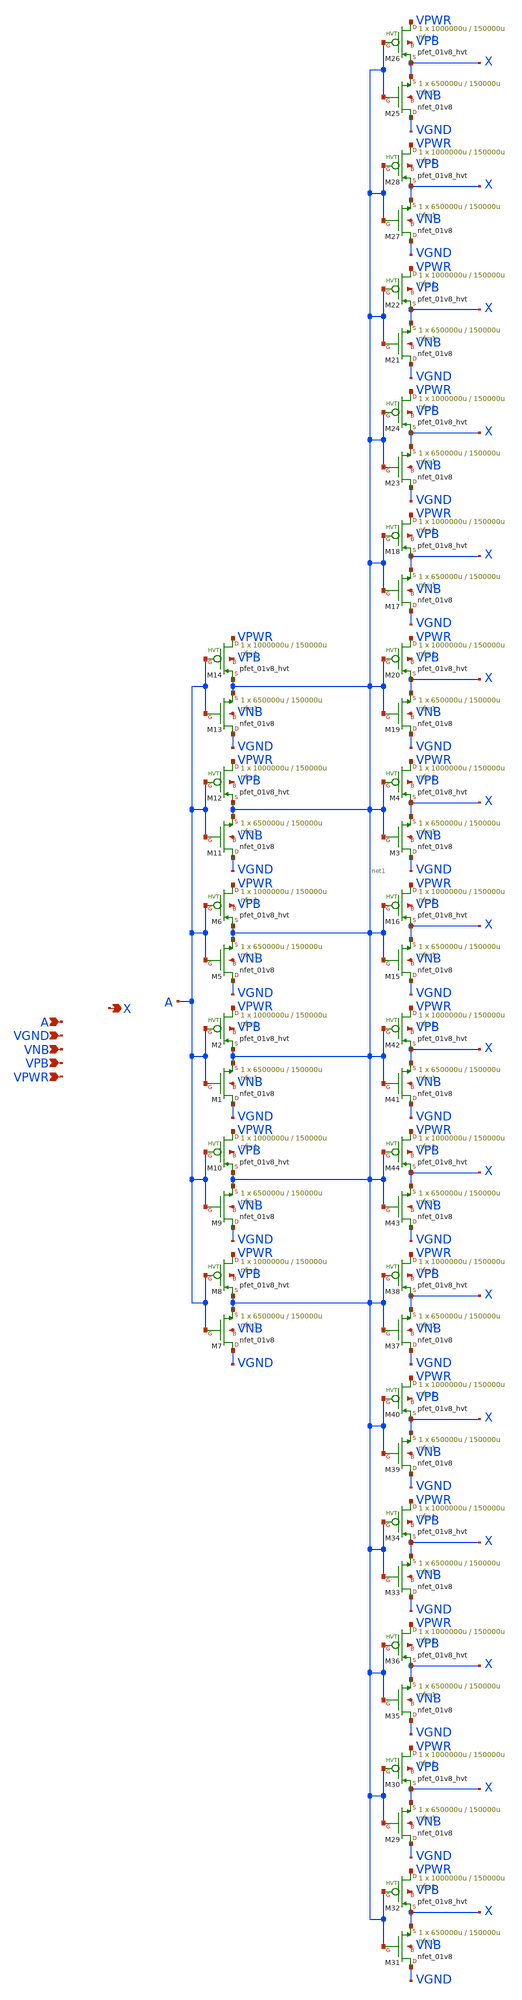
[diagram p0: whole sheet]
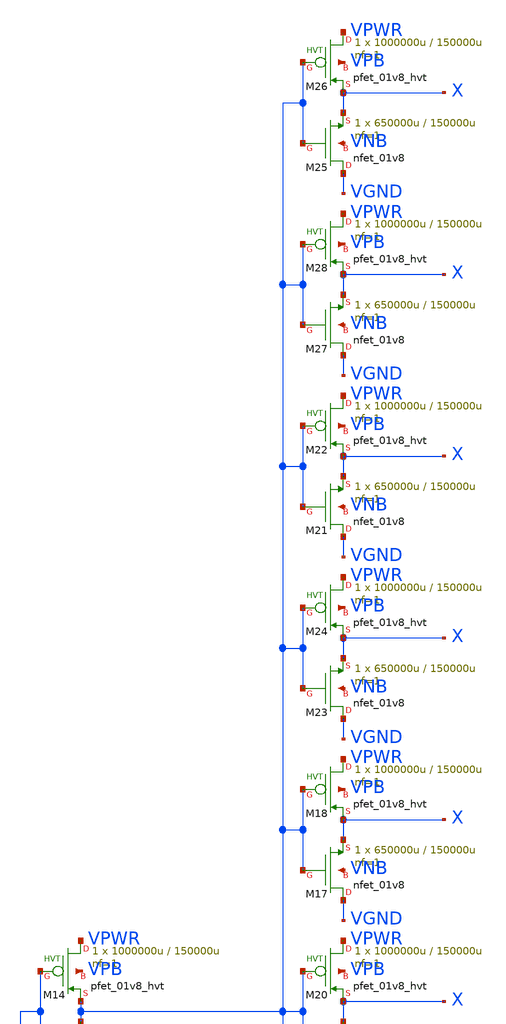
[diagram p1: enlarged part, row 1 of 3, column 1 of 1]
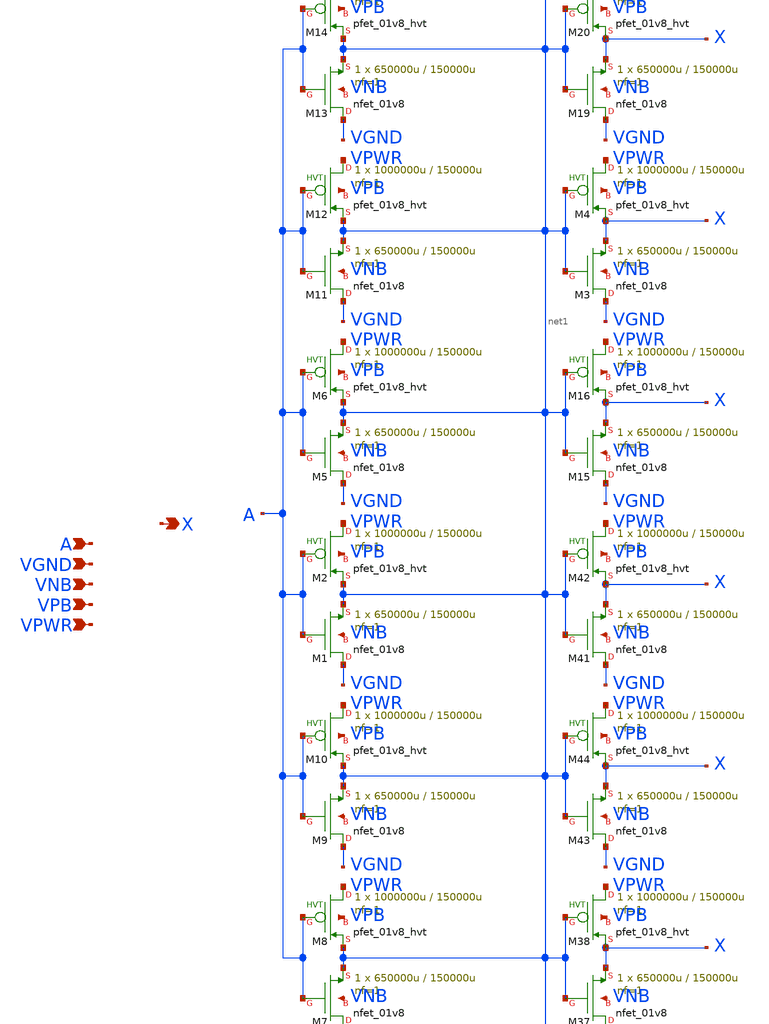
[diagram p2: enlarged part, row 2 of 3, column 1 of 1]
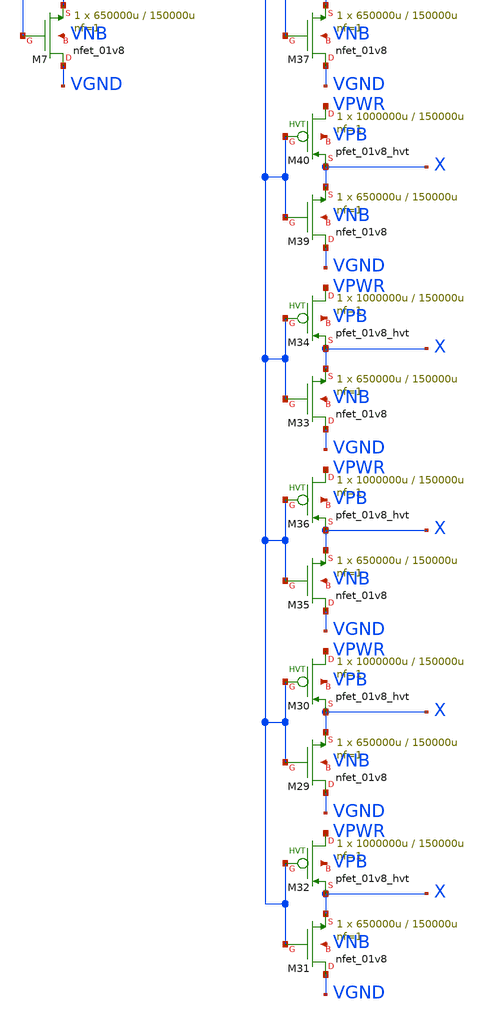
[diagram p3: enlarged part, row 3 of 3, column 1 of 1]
** sch_path: schematics/buf/sky130_fd_sc_hd__buf_16.sch
**.subckt sky130_fd_sc_hd__buf_16 A VGND VNB VPB VPWR X
*.ipin A
*.ipin VGND
*.ipin VNB
*.ipin VPB
*.ipin VPWR
*.opin X
XM1 VGND A net1 VNB sky130_fd_pr__nfet_01v8 L=150000u W=650000u nf=1 ad='int((1 + 1)/2) * 650000u / 1 * 0.29'
+ as='int((1 + 2)/2) * 650000u / 1 * 0.29' pd='2*int((1 + 1)/2) * (650000u / 1 + 0.29)' ps='2*int((1 + 2)/2) * (650000u / 1 + 0.29)'
+ nrd='0.29 / 650000u ' nrs='0.29 / 650000u ' sa=0 sb=0 sd=0 mult=1 m=1
XM2 VPWR A net1 VPB sky130_fd_pr__pfet_01v8_hvt L=150000u W=1000000u nf=1 ad='int((1 + 1)/2) * 1000000u / 1 * 0.29'
+ as='int((1 + 2)/2) * 1000000u / 1 * 0.29' pd='2*int((1 + 1)/2) * (1000000u / 1 + 0.29)' ps='2*int((1 + 2)/2) * (1000000u / 1 + 0.29)'
+ nrd='0.29 / 1000000u ' nrs='0.29 / 1000000u ' sa=0 sb=0 sd=0 mult=1 m=1
XM3 VGND net1 X VNB sky130_fd_pr__nfet_01v8 L=150000u W=650000u nf=1 ad='int((1 + 1)/2) * 650000u / 1 * 0.29'
+ as='int((1 + 2)/2) * 650000u / 1 * 0.29' pd='2*int((1 + 1)/2) * (650000u / 1 + 0.29)' ps='2*int((1 + 2)/2) * (650000u / 1 + 0.29)'
+ nrd='0.29 / 650000u ' nrs='0.29 / 650000u ' sa=0 sb=0 sd=0 mult=1 m=1
XM4 VPWR net1 X VPB sky130_fd_pr__pfet_01v8_hvt L=150000u W=1000000u nf=1 ad='int((1 + 1)/2) * 1000000u / 1 * 0.29'
+ as='int((1 + 2)/2) * 1000000u / 1 * 0.29' pd='2*int((1 + 1)/2) * (1000000u / 1 + 0.29)' ps='2*int((1 + 2)/2) * (1000000u / 1 + 0.29)'
+ nrd='0.29 / 1000000u ' nrs='0.29 / 1000000u ' sa=0 sb=0 sd=0 mult=1 m=1
XM5 VGND A net1 VNB sky130_fd_pr__nfet_01v8 L=150000u W=650000u nf=1 ad='int((1 + 1)/2) * 650000u / 1 * 0.29'
+ as='int((1 + 2)/2) * 650000u / 1 * 0.29' pd='2*int((1 + 1)/2) * (650000u / 1 + 0.29)' ps='2*int((1 + 2)/2) * (650000u / 1 + 0.29)'
+ nrd='0.29 / 650000u ' nrs='0.29 / 650000u ' sa=0 sb=0 sd=0 mult=1 m=1
XM6 VPWR A net1 VPB sky130_fd_pr__pfet_01v8_hvt L=150000u W=1000000u nf=1 ad='int((1 + 1)/2) * 1000000u / 1 * 0.29'
+ as='int((1 + 2)/2) * 1000000u / 1 * 0.29' pd='2*int((1 + 1)/2) * (1000000u / 1 + 0.29)' ps='2*int((1 + 2)/2) * (1000000u / 1 + 0.29)'
+ nrd='0.29 / 1000000u ' nrs='0.29 / 1000000u ' sa=0 sb=0 sd=0 mult=1 m=1
XM7 VGND A net1 VNB sky130_fd_pr__nfet_01v8 L=150000u W=650000u nf=1 ad='int((1 + 1)/2) * 650000u / 1 * 0.29'
+ as='int((1 + 2)/2) * 650000u / 1 * 0.29' pd='2*int((1 + 1)/2) * (650000u / 1 + 0.29)' ps='2*int((1 + 2)/2) * (650000u / 1 + 0.29)'
+ nrd='0.29 / 650000u ' nrs='0.29 / 650000u ' sa=0 sb=0 sd=0 mult=1 m=1
XM8 VPWR A net1 VPB sky130_fd_pr__pfet_01v8_hvt L=150000u W=1000000u nf=1 ad='int((1 + 1)/2) * 1000000u / 1 * 0.29'
+ as='int((1 + 2)/2) * 1000000u / 1 * 0.29' pd='2*int((1 + 1)/2) * (1000000u / 1 + 0.29)' ps='2*int((1 + 2)/2) * (1000000u / 1 + 0.29)'
+ nrd='0.29 / 1000000u ' nrs='0.29 / 1000000u ' sa=0 sb=0 sd=0 mult=1 m=1
XM9 VGND A net1 VNB sky130_fd_pr__nfet_01v8 L=150000u W=650000u nf=1 ad='int((1 + 1)/2) * 650000u / 1 * 0.29'
+ as='int((1 + 2)/2) * 650000u / 1 * 0.29' pd='2*int((1 + 1)/2) * (650000u / 1 + 0.29)' ps='2*int((1 + 2)/2) * (650000u / 1 + 0.29)'
+ nrd='0.29 / 650000u ' nrs='0.29 / 650000u ' sa=0 sb=0 sd=0 mult=1 m=1
XM10 VPWR A net1 VPB sky130_fd_pr__pfet_01v8_hvt L=150000u W=1000000u nf=1 ad='int((1 + 1)/2) * 1000000u / 1 * 0.29'
+ as='int((1 + 2)/2) * 1000000u / 1 * 0.29' pd='2*int((1 + 1)/2) * (1000000u / 1 + 0.29)' ps='2*int((1 + 2)/2) * (1000000u / 1 + 0.29)'
+ nrd='0.29 / 1000000u ' nrs='0.29 / 1000000u ' sa=0 sb=0 sd=0 mult=1 m=1
XM11 VGND A net1 VNB sky130_fd_pr__nfet_01v8 L=150000u W=650000u nf=1 ad='int((1 + 1)/2) * 650000u / 1 * 0.29'
+ as='int((1 + 2)/2) * 650000u / 1 * 0.29' pd='2*int((1 + 1)/2) * (650000u / 1 + 0.29)' ps='2*int((1 + 2)/2) * (650000u / 1 + 0.29)'
+ nrd='0.29 / 650000u ' nrs='0.29 / 650000u ' sa=0 sb=0 sd=0 mult=1 m=1
XM12 VPWR A net1 VPB sky130_fd_pr__pfet_01v8_hvt L=150000u W=1000000u nf=1 ad='int((1 + 1)/2) * 1000000u / 1 * 0.29'
+ as='int((1 + 2)/2) * 1000000u / 1 * 0.29' pd='2*int((1 + 1)/2) * (1000000u / 1 + 0.29)' ps='2*int((1 + 2)/2) * (1000000u / 1 + 0.29)'
+ nrd='0.29 / 1000000u ' nrs='0.29 / 1000000u ' sa=0 sb=0 sd=0 mult=1 m=1
XM13 VGND A net1 VNB sky130_fd_pr__nfet_01v8 L=150000u W=650000u nf=1 ad='int((1 + 1)/2) * 650000u / 1 * 0.29'
+ as='int((1 + 2)/2) * 650000u / 1 * 0.29' pd='2*int((1 + 1)/2) * (650000u / 1 + 0.29)' ps='2*int((1 + 2)/2) * (650000u / 1 + 0.29)'
+ nrd='0.29 / 650000u ' nrs='0.29 / 650000u ' sa=0 sb=0 sd=0 mult=1 m=1
XM14 VPWR A net1 VPB sky130_fd_pr__pfet_01v8_hvt L=150000u W=1000000u nf=1 ad='int((1 + 1)/2) * 1000000u / 1 * 0.29'
+ as='int((1 + 2)/2) * 1000000u / 1 * 0.29' pd='2*int((1 + 1)/2) * (1000000u / 1 + 0.29)' ps='2*int((1 + 2)/2) * (1000000u / 1 + 0.29)'
+ nrd='0.29 / 1000000u ' nrs='0.29 / 1000000u ' sa=0 sb=0 sd=0 mult=1 m=1
XM15 VGND net1 X VNB sky130_fd_pr__nfet_01v8 L=150000u W=650000u nf=1 ad='int((1 + 1)/2) * 650000u / 1 * 0.29'
+ as='int((1 + 2)/2) * 650000u / 1 * 0.29' pd='2*int((1 + 1)/2) * (650000u / 1 + 0.29)' ps='2*int((1 + 2)/2) * (650000u / 1 + 0.29)'
+ nrd='0.29 / 650000u ' nrs='0.29 / 650000u ' sa=0 sb=0 sd=0 mult=1 m=1
XM16 VPWR net1 X VPB sky130_fd_pr__pfet_01v8_hvt L=150000u W=1000000u nf=1 ad='int((1 + 1)/2) * 1000000u / 1 * 0.29'
+ as='int((1 + 2)/2) * 1000000u / 1 * 0.29' pd='2*int((1 + 1)/2) * (1000000u / 1 + 0.29)' ps='2*int((1 + 2)/2) * (1000000u / 1 + 0.29)'
+ nrd='0.29 / 1000000u ' nrs='0.29 / 1000000u ' sa=0 sb=0 sd=0 mult=1 m=1
XM17 VGND net1 X VNB sky130_fd_pr__nfet_01v8 L=150000u W=650000u nf=1 ad='int((1 + 1)/2) * 650000u / 1 * 0.29'
+ as='int((1 + 2)/2) * 650000u / 1 * 0.29' pd='2*int((1 + 1)/2) * (650000u / 1 + 0.29)' ps='2*int((1 + 2)/2) * (650000u / 1 + 0.29)'
+ nrd='0.29 / 650000u ' nrs='0.29 / 650000u ' sa=0 sb=0 sd=0 mult=1 m=1
XM18 VPWR net1 X VPB sky130_fd_pr__pfet_01v8_hvt L=150000u W=1000000u nf=1 ad='int((1 + 1)/2) * 1000000u / 1 * 0.29'
+ as='int((1 + 2)/2) * 1000000u / 1 * 0.29' pd='2*int((1 + 1)/2) * (1000000u / 1 + 0.29)' ps='2*int((1 + 2)/2) * (1000000u / 1 + 0.29)'
+ nrd='0.29 / 1000000u ' nrs='0.29 / 1000000u ' sa=0 sb=0 sd=0 mult=1 m=1
XM19 VGND net1 X VNB sky130_fd_pr__nfet_01v8 L=150000u W=650000u nf=1 ad='int((1 + 1)/2) * 650000u / 1 * 0.29'
+ as='int((1 + 2)/2) * 650000u / 1 * 0.29' pd='2*int((1 + 1)/2) * (650000u / 1 + 0.29)' ps='2*int((1 + 2)/2) * (650000u / 1 + 0.29)'
+ nrd='0.29 / 650000u ' nrs='0.29 / 650000u ' sa=0 sb=0 sd=0 mult=1 m=1
XM20 VPWR net1 X VPB sky130_fd_pr__pfet_01v8_hvt L=150000u W=1000000u nf=1 ad='int((1 + 1)/2) * 1000000u / 1 * 0.29'
+ as='int((1 + 2)/2) * 1000000u / 1 * 0.29' pd='2*int((1 + 1)/2) * (1000000u / 1 + 0.29)' ps='2*int((1 + 2)/2) * (1000000u / 1 + 0.29)'
+ nrd='0.29 / 1000000u ' nrs='0.29 / 1000000u ' sa=0 sb=0 sd=0 mult=1 m=1
XM21 VGND net1 X VNB sky130_fd_pr__nfet_01v8 L=150000u W=650000u nf=1 ad='int((1 + 1)/2) * 650000u / 1 * 0.29'
+ as='int((1 + 2)/2) * 650000u / 1 * 0.29' pd='2*int((1 + 1)/2) * (650000u / 1 + 0.29)' ps='2*int((1 + 2)/2) * (650000u / 1 + 0.29)'
+ nrd='0.29 / 650000u ' nrs='0.29 / 650000u ' sa=0 sb=0 sd=0 mult=1 m=1
XM22 VPWR net1 X VPB sky130_fd_pr__pfet_01v8_hvt L=150000u W=1000000u nf=1 ad='int((1 + 1)/2) * 1000000u / 1 * 0.29'
+ as='int((1 + 2)/2) * 1000000u / 1 * 0.29' pd='2*int((1 + 1)/2) * (1000000u / 1 + 0.29)' ps='2*int((1 + 2)/2) * (1000000u / 1 + 0.29)'
+ nrd='0.29 / 1000000u ' nrs='0.29 / 1000000u ' sa=0 sb=0 sd=0 mult=1 m=1
XM23 VGND net1 X VNB sky130_fd_pr__nfet_01v8 L=150000u W=650000u nf=1 ad='int((1 + 1)/2) * 650000u / 1 * 0.29'
+ as='int((1 + 2)/2) * 650000u / 1 * 0.29' pd='2*int((1 + 1)/2) * (650000u / 1 + 0.29)' ps='2*int((1 + 2)/2) * (650000u / 1 + 0.29)'
+ nrd='0.29 / 650000u ' nrs='0.29 / 650000u ' sa=0 sb=0 sd=0 mult=1 m=1
XM24 VPWR net1 X VPB sky130_fd_pr__pfet_01v8_hvt L=150000u W=1000000u nf=1 ad='int((1 + 1)/2) * 1000000u / 1 * 0.29'
+ as='int((1 + 2)/2) * 1000000u / 1 * 0.29' pd='2*int((1 + 1)/2) * (1000000u / 1 + 0.29)' ps='2*int((1 + 2)/2) * (1000000u / 1 + 0.29)'
+ nrd='0.29 / 1000000u ' nrs='0.29 / 1000000u ' sa=0 sb=0 sd=0 mult=1 m=1
XM25 VGND net1 X VNB sky130_fd_pr__nfet_01v8 L=150000u W=650000u nf=1 ad='int((1 + 1)/2) * 650000u / 1 * 0.29'
+ as='int((1 + 2)/2) * 650000u / 1 * 0.29' pd='2*int((1 + 1)/2) * (650000u / 1 + 0.29)' ps='2*int((1 + 2)/2) * (650000u / 1 + 0.29)'
+ nrd='0.29 / 650000u ' nrs='0.29 / 650000u ' sa=0 sb=0 sd=0 mult=1 m=1
XM26 VPWR net1 X VPB sky130_fd_pr__pfet_01v8_hvt L=150000u W=1000000u nf=1 ad='int((1 + 1)/2) * 1000000u / 1 * 0.29'
+ as='int((1 + 2)/2) * 1000000u / 1 * 0.29' pd='2*int((1 + 1)/2) * (1000000u / 1 + 0.29)' ps='2*int((1 + 2)/2) * (1000000u / 1 + 0.29)'
+ nrd='0.29 / 1000000u ' nrs='0.29 / 1000000u ' sa=0 sb=0 sd=0 mult=1 m=1
XM27 VGND net1 X VNB sky130_fd_pr__nfet_01v8 L=150000u W=650000u nf=1 ad='int((1 + 1)/2) * 650000u / 1 * 0.29'
+ as='int((1 + 2)/2) * 650000u / 1 * 0.29' pd='2*int((1 + 1)/2) * (650000u / 1 + 0.29)' ps='2*int((1 + 2)/2) * (650000u / 1 + 0.29)'
+ nrd='0.29 / 650000u ' nrs='0.29 / 650000u ' sa=0 sb=0 sd=0 mult=1 m=1
XM28 VPWR net1 X VPB sky130_fd_pr__pfet_01v8_hvt L=150000u W=1000000u nf=1 ad='int((1 + 1)/2) * 1000000u / 1 * 0.29'
+ as='int((1 + 2)/2) * 1000000u / 1 * 0.29' pd='2*int((1 + 1)/2) * (1000000u / 1 + 0.29)' ps='2*int((1 + 2)/2) * (1000000u / 1 + 0.29)'
+ nrd='0.29 / 1000000u ' nrs='0.29 / 1000000u ' sa=0 sb=0 sd=0 mult=1 m=1
XM29 VGND net1 X VNB sky130_fd_pr__nfet_01v8 L=150000u W=650000u nf=1 ad='int((1 + 1)/2) * 650000u / 1 * 0.29'
+ as='int((1 + 2)/2) * 650000u / 1 * 0.29' pd='2*int((1 + 1)/2) * (650000u / 1 + 0.29)' ps='2*int((1 + 2)/2) * (650000u / 1 + 0.29)'
+ nrd='0.29 / 650000u ' nrs='0.29 / 650000u ' sa=0 sb=0 sd=0 mult=1 m=1
XM30 VPWR net1 X VPB sky130_fd_pr__pfet_01v8_hvt L=150000u W=1000000u nf=1 ad='int((1 + 1)/2) * 1000000u / 1 * 0.29'
+ as='int((1 + 2)/2) * 1000000u / 1 * 0.29' pd='2*int((1 + 1)/2) * (1000000u / 1 + 0.29)' ps='2*int((1 + 2)/2) * (1000000u / 1 + 0.29)'
+ nrd='0.29 / 1000000u ' nrs='0.29 / 1000000u ' sa=0 sb=0 sd=0 mult=1 m=1
XM31 VGND net1 X VNB sky130_fd_pr__nfet_01v8 L=150000u W=650000u nf=1 ad='int((1 + 1)/2) * 650000u / 1 * 0.29'
+ as='int((1 + 2)/2) * 650000u / 1 * 0.29' pd='2*int((1 + 1)/2) * (650000u / 1 + 0.29)' ps='2*int((1 + 2)/2) * (650000u / 1 + 0.29)'
+ nrd='0.29 / 650000u ' nrs='0.29 / 650000u ' sa=0 sb=0 sd=0 mult=1 m=1
XM32 VPWR net1 X VPB sky130_fd_pr__pfet_01v8_hvt L=150000u W=1000000u nf=1 ad='int((1 + 1)/2) * 1000000u / 1 * 0.29'
+ as='int((1 + 2)/2) * 1000000u / 1 * 0.29' pd='2*int((1 + 1)/2) * (1000000u / 1 + 0.29)' ps='2*int((1 + 2)/2) * (1000000u / 1 + 0.29)'
+ nrd='0.29 / 1000000u ' nrs='0.29 / 1000000u ' sa=0 sb=0 sd=0 mult=1 m=1
XM33 VGND net1 X VNB sky130_fd_pr__nfet_01v8 L=150000u W=650000u nf=1 ad='int((1 + 1)/2) * 650000u / 1 * 0.29'
+ as='int((1 + 2)/2) * 650000u / 1 * 0.29' pd='2*int((1 + 1)/2) * (650000u / 1 + 0.29)' ps='2*int((1 + 2)/2) * (650000u / 1 + 0.29)'
+ nrd='0.29 / 650000u ' nrs='0.29 / 650000u ' sa=0 sb=0 sd=0 mult=1 m=1
XM34 VPWR net1 X VPB sky130_fd_pr__pfet_01v8_hvt L=150000u W=1000000u nf=1 ad='int((1 + 1)/2) * 1000000u / 1 * 0.29'
+ as='int((1 + 2)/2) * 1000000u / 1 * 0.29' pd='2*int((1 + 1)/2) * (1000000u / 1 + 0.29)' ps='2*int((1 + 2)/2) * (1000000u / 1 + 0.29)'
+ nrd='0.29 / 1000000u ' nrs='0.29 / 1000000u ' sa=0 sb=0 sd=0 mult=1 m=1
XM35 VGND net1 X VNB sky130_fd_pr__nfet_01v8 L=150000u W=650000u nf=1 ad='int((1 + 1)/2) * 650000u / 1 * 0.29'
+ as='int((1 + 2)/2) * 650000u / 1 * 0.29' pd='2*int((1 + 1)/2) * (650000u / 1 + 0.29)' ps='2*int((1 + 2)/2) * (650000u / 1 + 0.29)'
+ nrd='0.29 / 650000u ' nrs='0.29 / 650000u ' sa=0 sb=0 sd=0 mult=1 m=1
XM36 VPWR net1 X VPB sky130_fd_pr__pfet_01v8_hvt L=150000u W=1000000u nf=1 ad='int((1 + 1)/2) * 1000000u / 1 * 0.29'
+ as='int((1 + 2)/2) * 1000000u / 1 * 0.29' pd='2*int((1 + 1)/2) * (1000000u / 1 + 0.29)' ps='2*int((1 + 2)/2) * (1000000u / 1 + 0.29)'
+ nrd='0.29 / 1000000u ' nrs='0.29 / 1000000u ' sa=0 sb=0 sd=0 mult=1 m=1
XM37 VGND net1 X VNB sky130_fd_pr__nfet_01v8 L=150000u W=650000u nf=1 ad='int((1 + 1)/2) * 650000u / 1 * 0.29'
+ as='int((1 + 2)/2) * 650000u / 1 * 0.29' pd='2*int((1 + 1)/2) * (650000u / 1 + 0.29)' ps='2*int((1 + 2)/2) * (650000u / 1 + 0.29)'
+ nrd='0.29 / 650000u ' nrs='0.29 / 650000u ' sa=0 sb=0 sd=0 mult=1 m=1
XM38 VPWR net1 X VPB sky130_fd_pr__pfet_01v8_hvt L=150000u W=1000000u nf=1 ad='int((1 + 1)/2) * 1000000u / 1 * 0.29'
+ as='int((1 + 2)/2) * 1000000u / 1 * 0.29' pd='2*int((1 + 1)/2) * (1000000u / 1 + 0.29)' ps='2*int((1 + 2)/2) * (1000000u / 1 + 0.29)'
+ nrd='0.29 / 1000000u ' nrs='0.29 / 1000000u ' sa=0 sb=0 sd=0 mult=1 m=1
XM39 VGND net1 X VNB sky130_fd_pr__nfet_01v8 L=150000u W=650000u nf=1 ad='int((1 + 1)/2) * 650000u / 1 * 0.29'
+ as='int((1 + 2)/2) * 650000u / 1 * 0.29' pd='2*int((1 + 1)/2) * (650000u / 1 + 0.29)' ps='2*int((1 + 2)/2) * (650000u / 1 + 0.29)'
+ nrd='0.29 / 650000u ' nrs='0.29 / 650000u ' sa=0 sb=0 sd=0 mult=1 m=1
XM40 VPWR net1 X VPB sky130_fd_pr__pfet_01v8_hvt L=150000u W=1000000u nf=1 ad='int((1 + 1)/2) * 1000000u / 1 * 0.29'
+ as='int((1 + 2)/2) * 1000000u / 1 * 0.29' pd='2*int((1 + 1)/2) * (1000000u / 1 + 0.29)' ps='2*int((1 + 2)/2) * (1000000u / 1 + 0.29)'
+ nrd='0.29 / 1000000u ' nrs='0.29 / 1000000u ' sa=0 sb=0 sd=0 mult=1 m=1
XM41 VGND net1 X VNB sky130_fd_pr__nfet_01v8 L=150000u W=650000u nf=1 ad='int((1 + 1)/2) * 650000u / 1 * 0.29'
+ as='int((1 + 2)/2) * 650000u / 1 * 0.29' pd='2*int((1 + 1)/2) * (650000u / 1 + 0.29)' ps='2*int((1 + 2)/2) * (650000u / 1 + 0.29)'
+ nrd='0.29 / 650000u ' nrs='0.29 / 650000u ' sa=0 sb=0 sd=0 mult=1 m=1
XM42 VPWR net1 X VPB sky130_fd_pr__pfet_01v8_hvt L=150000u W=1000000u nf=1 ad='int((1 + 1)/2) * 1000000u / 1 * 0.29'
+ as='int((1 + 2)/2) * 1000000u / 1 * 0.29' pd='2*int((1 + 1)/2) * (1000000u / 1 + 0.29)' ps='2*int((1 + 2)/2) * (1000000u / 1 + 0.29)'
+ nrd='0.29 / 1000000u ' nrs='0.29 / 1000000u ' sa=0 sb=0 sd=0 mult=1 m=1
XM43 VGND net1 X VNB sky130_fd_pr__nfet_01v8 L=150000u W=650000u nf=1 ad='int((1 + 1)/2) * 650000u / 1 * 0.29'
+ as='int((1 + 2)/2) * 650000u / 1 * 0.29' pd='2*int((1 + 1)/2) * (650000u / 1 + 0.29)' ps='2*int((1 + 2)/2) * (650000u / 1 + 0.29)'
+ nrd='0.29 / 650000u ' nrs='0.29 / 650000u ' sa=0 sb=0 sd=0 mult=1 m=1
XM44 VPWR net1 X VPB sky130_fd_pr__pfet_01v8_hvt L=150000u W=1000000u nf=1 ad='int((1 + 1)/2) * 1000000u / 1 * 0.29'
+ as='int((1 + 2)/2) * 1000000u / 1 * 0.29' pd='2*int((1 + 1)/2) * (1000000u / 1 + 0.29)' ps='2*int((1 + 2)/2) * (1000000u / 1 + 0.29)'
+ nrd='0.29 / 1000000u ' nrs='0.29 / 1000000u ' sa=0 sb=0 sd=0 mult=1 m=1
**.ends
.end
